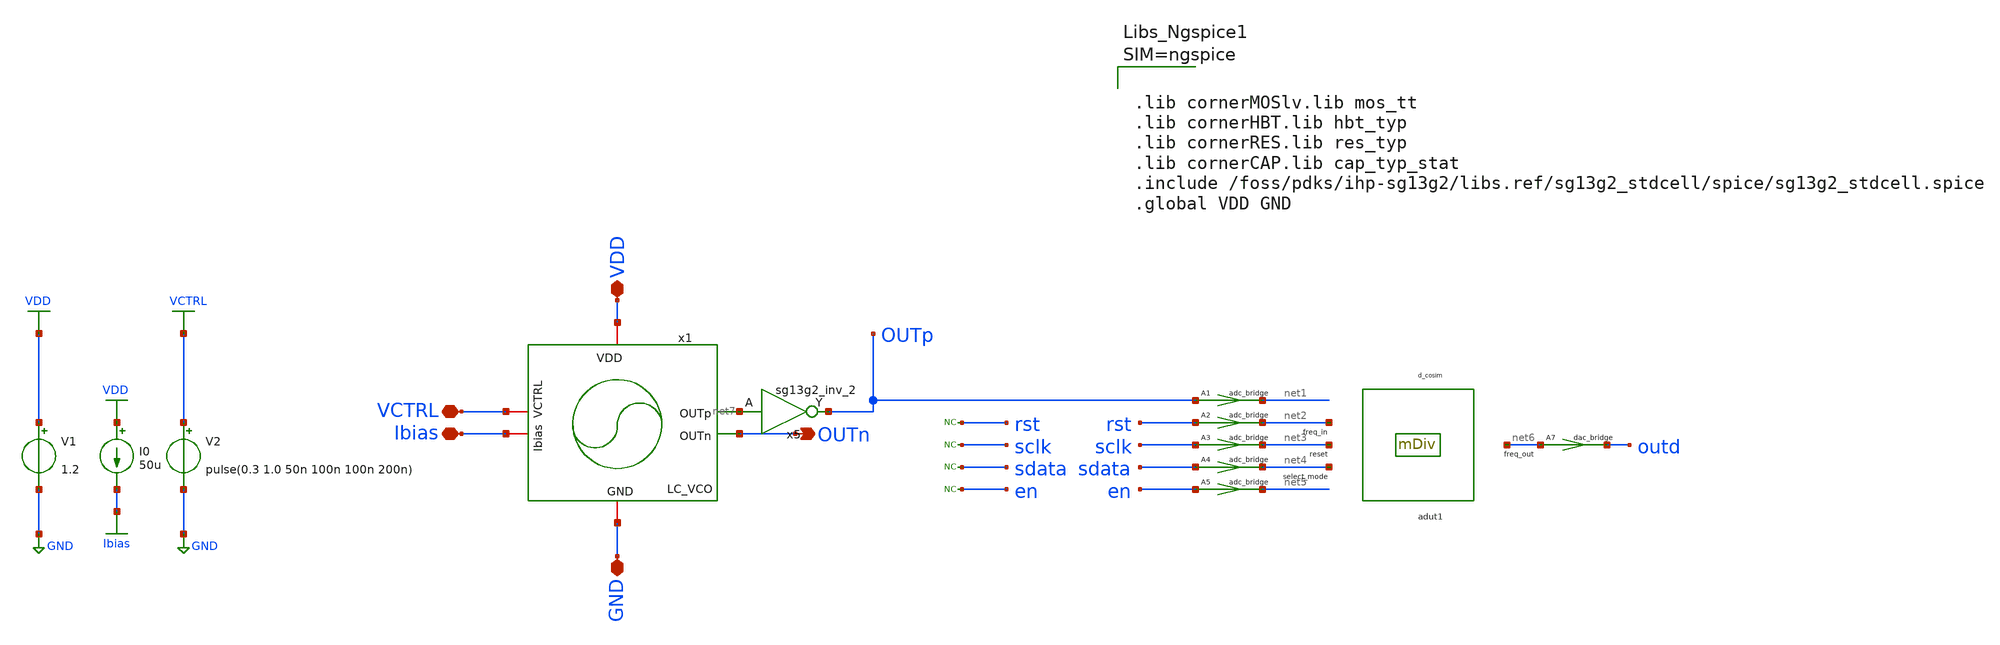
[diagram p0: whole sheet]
** sch_path: schematic/blocks/top-pll/LCVCO_DSM_tb.sch
**.subckt LCVCO_DSM_tb OUTn VDD VCTRL GND Ibias
*.opin OUTn
*.iopin VDD
*.iopin VCTRL
*.iopin GND
*.iopin Ibias
* noconn rst
* noconn sclk
* noconn sdata
* noconn en
V1 VDD GND 1.2
V2 VCTRL GND pulse(0.3 1.0 50n 100n 100n 200n)
I0 VDD Ibias 50u
x5 OUTp net7 VDD GND sg13g2_inv_2
adut1 [ net2 net3 net4 ] [ net6 ] null dut
.model dut d_cosim simulation=./../Frequency_Divider_240_248.so
A7 [ net6 ] [ outd ] dac1
.model dac1 dac_bridge out_low=0 out_high=1.2
A1 [ OUTp ] [ net1 ] adc1
.model adc1 adc_bridge in_low=0.4 in_high=0.6
A2 [ rst ] [ net2 ] adc1
.model adc1 adc_bridge in_low=0.4 in_high=0.6
A3 [ sclk ] [ net3 ] adc1
.model adc1 adc_bridge in_low=0.4 in_high=0.6
A4 [ sdata ] [ net4 ] adc1
.model adc1 adc_bridge in_low=0.4 in_high=0.6
A5 [ en ] [ net5 ] adc1
.model adc1 adc_bridge in_low=0.4 in_high=0.6
x1 VDD net7 OUTn Ibias VCTRL GND LC_VCO
**** begin user architecture code



.include ./IHP_4nH_Inductor.spice
.param temp=27
.control
save V(VCTRL) V(OUTp) V(outd) V(sdata) V(sclk) V(en) V(rst)
.options maxstep=50p reltol=1e-3 abstol=1e-6

*.ic v(OUTp)=0.6
tran 5p 400n
remzerovec

* Perform FFT on output
*fft v(OUTp)
*let vmag = db(mag(v(OUTp)))
*plot vmag xlabel 'Frequency (Hz)' xlimit 0 5G

* Save transient waveform to raw file
write LCVCO_DSM.raw

*quit 0
.endc


* to generate following file copy stimuli.test
* to the simulation directory and run simulation -> Utile Stimuli Editor (GUI),
* and press 'Translate'
.include stimuli_test.cir






.lib cornerMOSlv.lib mos_tt
.lib cornerHBT.lib hbt_typ
.lib cornerRES.lib res_typ
.lib cornerCAP.lib cap_typ_stat
.include /foss/pdks/ihp-sg13g2/libs.ref/sg13g2_stdcell/spice/sg13g2_stdcell.spice
.global VDD GND



**** end user architecture code
**.ends
.GLOBAL GND
.GLOBAL VDD
.GLOBAL VCTRL
.GLOBAL Ibias
.end
